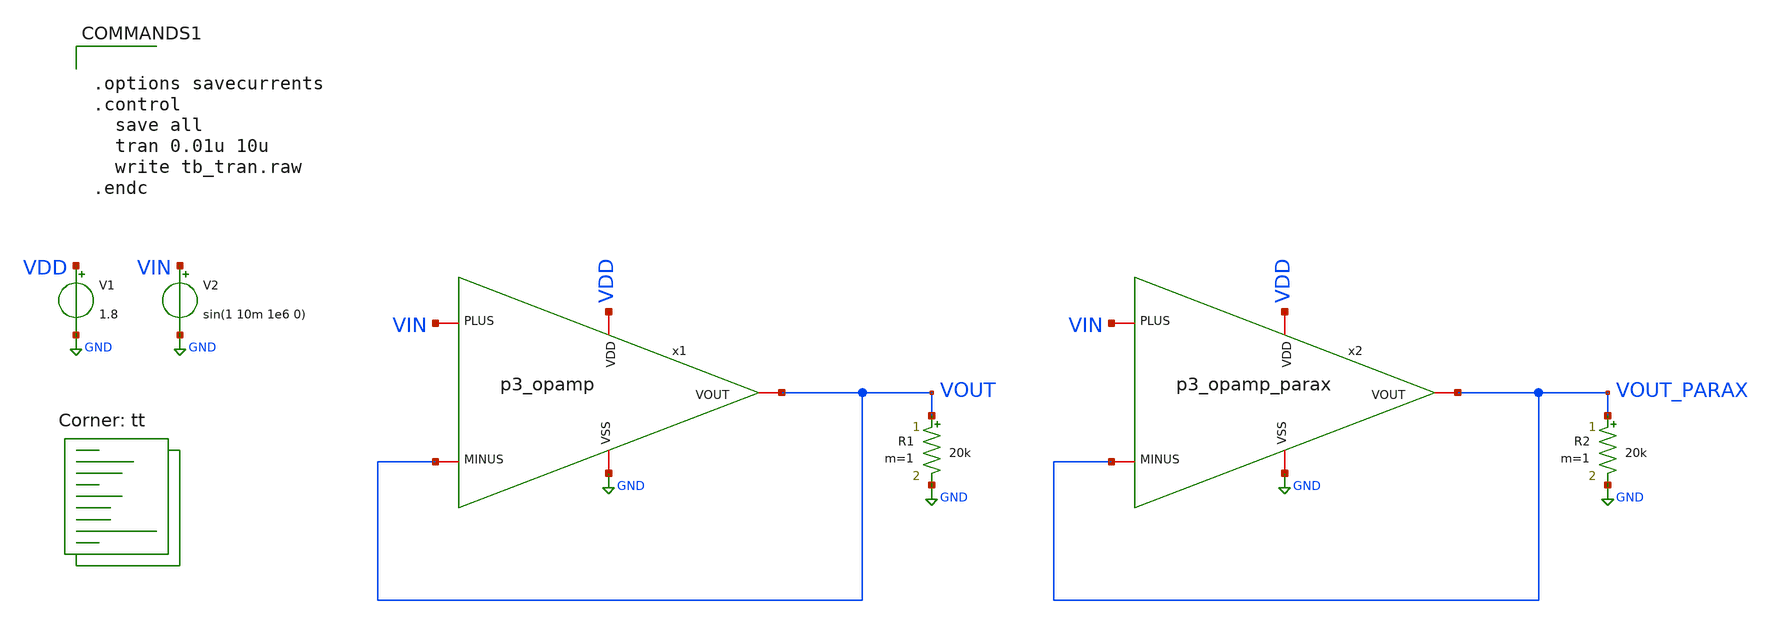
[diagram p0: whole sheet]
** sch_path: xschem/p3_tb_tran.sch
**.subckt p3_tb_tran
V1 VDD GND 1.8
V2 VIN GND sin(1 10m 1e6 0)
R1 VOUT GND 20k m=1
x1 VDD VOUT VIN VOUT GND p3_opamp
R2 VOUT_PARAX GND 20k m=1
x2 VDD VOUT_PARAX VIN VOUT_PARAX GND p3_opamp_parax
**** begin user architecture code
.lib $::SKYWATER_MODELS/sky130.lib.spice tt


.options savecurrents
.control
  save all
  tran 0.01u 10u
  write tb_tran.raw
.endc


**** end user architecture code
**.ends

* expanding   symbol:  p3_opamp.sym # of pins=5
** sym_path: p3_opamp.sym
** sch_path: p3_opamp.sch
.subckt p3_opamp VDD MINUS PLUS VOUT VSS
*.iopin VDD
*.iopin VSS
*.iopin PLUS
*.iopin MINUS
*.iopin VOUT
XM3 VX VBIAS VSS VSS sky130_fd_pr__nfet_01v8 L=2 W=4 nf=1 ad='int((nf+1)/2) * W/nf * 0.29' as='int((nf+2)/2) * W/nf * 0.29'
+ pd='2*int((nf+1)/2) * (W/nf + 0.29)' ps='2*int((nf+2)/2) * (W/nf + 0.29)' nrd='0.29 / W' nrs='0.29 / W'
+ sa=0 sb=0 sd=0 mult=1 m=1
XM6 VBIAS VBIAS VSS VSS sky130_fd_pr__nfet_01v8 L=2 W=4 nf=1 ad='int((nf+1)/2) * W/nf * 0.29' as='int((nf+2)/2) * W/nf * 0.29'
+ pd='2*int((nf+1)/2) * (W/nf + 0.29)' ps='2*int((nf+2)/2) * (W/nf + 0.29)' nrd='0.29 / W' nrs='0.29 / W'
+ sa=0 sb=0 sd=0 mult=1 m=1
XM7 VOUT VBIAS VSS VSS sky130_fd_pr__nfet_01v8 L=2 W=7 nf=1 ad='int((nf+1)/2) * W/nf * 0.29' as='int((nf+2)/2) * W/nf * 0.29'
+ pd='2*int((nf+1)/2) * (W/nf + 0.29)' ps='2*int((nf+2)/2) * (W/nf + 0.29)' nrd='0.29 / W' nrs='0.29 / W'
+ sa=0 sb=0 sd=0 mult=1 m=1
XM8 VOUT V1 VDD VDD sky130_fd_pr__pfet_01v8 L=2 W=80 nf=1 ad='int((nf+1)/2) * W/nf * 0.29' as='int((nf+2)/2) * W/nf * 0.29'
+ pd='2*int((nf+1)/2) * (W/nf + 0.29)' ps='2*int((nf+2)/2) * (W/nf + 0.29)' nrd='0.29 / W' nrs='0.29 / W'
+ sa=0 sb=0 sd=0 mult=4 m=4
XR1 VBIAS VDD VSS sky130_fd_pr__res_xhigh_po_0p35 L=2.8 mult=1 m=1
XM2 V2 MINUS VX VSS sky130_fd_pr__nfet_01v8_lvt L=0.5 W=2.5 nf=1 ad='int((nf+1)/2) * W/nf * 0.29' as='int((nf+2)/2) * W/nf * 0.29'
+ pd='2*int((nf+1)/2) * (W/nf + 0.29)' ps='2*int((nf+2)/2) * (W/nf + 0.29)' nrd='0.29 / W' nrs='0.29 / W'
+ sa=0 sb=0 sd=0 mult=1 m=1
XM1 V1 PLUS VX VSS sky130_fd_pr__nfet_01v8_lvt L=0.5 W=2.5 nf=1 ad='int((nf+1)/2) * W/nf * 0.29' as='int((nf+2)/2) * W/nf * 0.29'
+ pd='2*int((nf+1)/2) * (W/nf + 0.29)' ps='2*int((nf+2)/2) * (W/nf + 0.29)' nrd='0.29 / W' nrs='0.29 / W'
+ sa=0 sb=0 sd=0 mult=1 m=1
XM4 V2 V2 VDD VDD sky130_fd_pr__pfet_01v8_lvt L=2 W=6 nf=1 ad='int((nf+1)/2) * W/nf * 0.29' as='int((nf+2)/2) * W/nf * 0.29'
+ pd='2*int((nf+1)/2) * (W/nf + 0.29)' ps='2*int((nf+2)/2) * (W/nf + 0.29)' nrd='0.29 / W' nrs='0.29 / W'
+ sa=0 sb=0 sd=0 mult=1 m=1
XM5 V1 V2 VDD VDD sky130_fd_pr__pfet_01v8_lvt L=2 W=6 nf=1 ad='int((nf+1)/2) * W/nf * 0.29' as='int((nf+2)/2) * W/nf * 0.29'
+ pd='2*int((nf+1)/2) * (W/nf + 0.29)' ps='2*int((nf+2)/2) * (W/nf + 0.29)' nrd='0.29 / W' nrs='0.29 / W'
+ sa=0 sb=0 sd=0 mult=1 m=1
.ends


* expanding   symbol:  p3_opamp_parax.sym # of pins=5
** sym_path: p3_opamp.sym
.include [file normalize ../mag/p3_opamp.sim.spice]
.GLOBAL GND
.end
